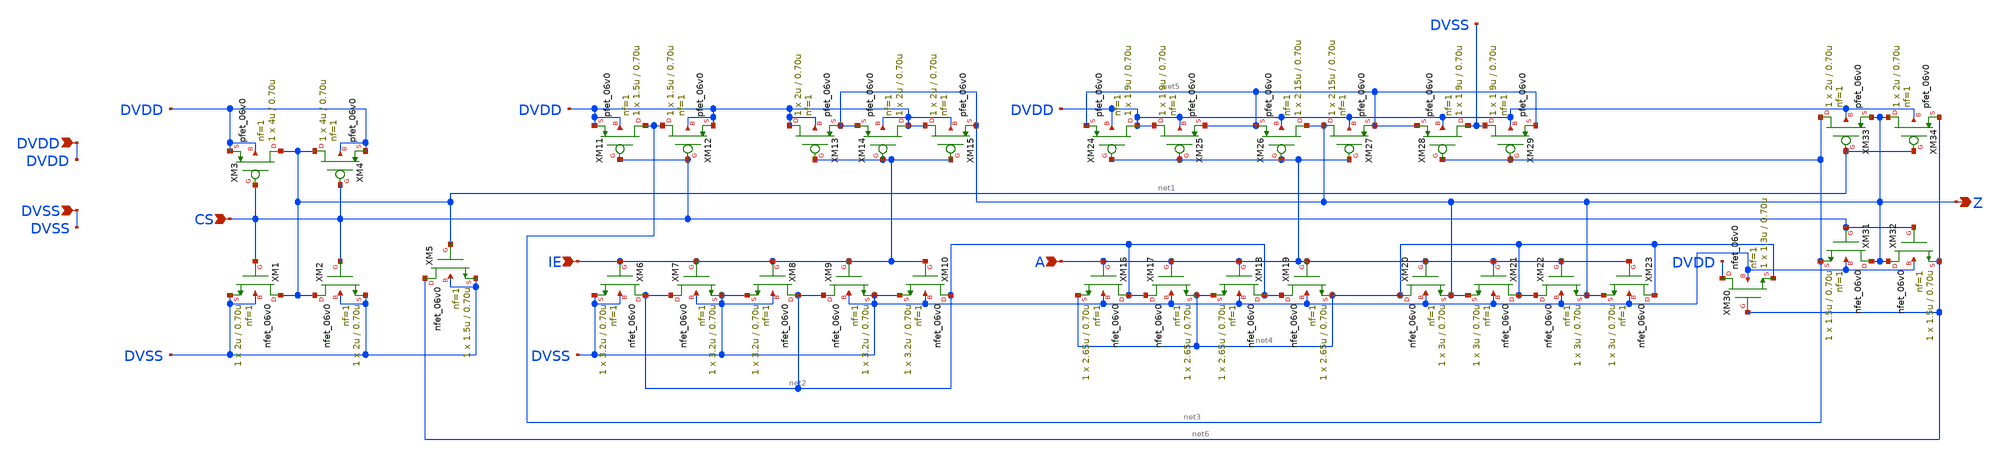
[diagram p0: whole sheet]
** sch_path: gf180mcu_fd_io__bi_24t/comp018green_in_cms_smt.sch
**.subckt comp018green_in_cms_smt CS IE Z A DVDD DVSS
*.ipin CS
*.ipin IE
*.opin Z
*.ipin A
*.ipin DVDD
*.ipin DVSS
XM1 net1 CS DVSS DVSS nfet_06v0 L=0.70u W=2u nf=1 ad='int((nf+1)/2) * W/nf * 0.18u' as='int((nf+2)/2) * W/nf * 0.18u'
+ pd='2*int((nf+1)/2) * (W/nf + 0.18u)' ps='2*int((nf+2)/2) * (W/nf + 0.18u)' nrd='0.18u / W' nrs='0.18u / W'
+ sa=0 sb=0 sd=0 m=1
XM2 net1 CS DVSS DVSS nfet_06v0 L=0.70u W=2u nf=1 ad='int((nf+1)/2) * W/nf * 0.18u' as='int((nf+2)/2) * W/nf * 0.18u'
+ pd='2*int((nf+1)/2) * (W/nf + 0.18u)' ps='2*int((nf+2)/2) * (W/nf + 0.18u)' nrd='0.18u / W' nrs='0.18u / W'
+ sa=0 sb=0 sd=0 m=1
XM3 net1 CS DVDD DVDD pfet_06v0 L=0.70u W=4u nf=1 ad='int((nf+1)/2) * W/nf * 0.18u' as='int((nf+2)/2) * W/nf * 0.18u'
+ pd='2*int((nf+1)/2) * (W/nf + 0.18u)' ps='2*int((nf+2)/2) * (W/nf + 0.18u)' nrd='0.18u / W' nrs='0.18u / W'
+ sa=0 sb=0 sd=0 m=1
XM4 net1 CS DVDD DVDD pfet_06v0 L=0.70u W=4u nf=1 ad='int((nf+1)/2) * W/nf * 0.18u' as='int((nf+2)/2) * W/nf * 0.18u'
+ pd='2*int((nf+1)/2) * (W/nf + 0.18u)' ps='2*int((nf+2)/2) * (W/nf + 0.18u)' nrd='0.18u / W' nrs='0.18u / W'
+ sa=0 sb=0 sd=0 m=1
XM5 net6 net1 DVSS DVSS nfet_06v0 L=0.70u W=1.5u nf=1 ad='int((nf+1)/2) * W/nf * 0.18u' as='int((nf+2)/2) * W/nf * 0.18u'
+ pd='2*int((nf+1)/2) * (W/nf + 0.18u)' ps='2*int((nf+2)/2) * (W/nf + 0.18u)' nrd='0.18u / W' nrs='0.18u / W'
+ sa=0 sb=0 sd=0 m=1
XM6 net2 IE DVSS DVSS nfet_06v0 L=0.70u W=3.2u nf=1 ad='int((nf+1)/2) * W/nf * 0.18u' as='int((nf+2)/2) * W/nf * 0.18u'
+ pd='2*int((nf+1)/2) * (W/nf + 0.18u)' ps='2*int((nf+2)/2) * (W/nf + 0.18u)' nrd='0.18u / W' nrs='0.18u / W'
+ sa=0 sb=0 sd=0 m=1
XM7 net2 IE DVSS DVSS nfet_06v0 L=0.70u W=3.2u nf=1 ad='int((nf+1)/2) * W/nf * 0.18u' as='int((nf+2)/2) * W/nf * 0.18u'
+ pd='2*int((nf+1)/2) * (W/nf + 0.18u)' ps='2*int((nf+2)/2) * (W/nf + 0.18u)' nrd='0.18u / W' nrs='0.18u / W'
+ sa=0 sb=0 sd=0 m=1
XM8 net2 IE DVSS DVSS nfet_06v0 L=0.70u W=3.2u nf=1 ad='int((nf+1)/2) * W/nf * 0.18u' as='int((nf+2)/2) * W/nf * 0.18u'
+ pd='2*int((nf+1)/2) * (W/nf + 0.18u)' ps='2*int((nf+2)/2) * (W/nf + 0.18u)' nrd='0.18u / W' nrs='0.18u / W'
+ sa=0 sb=0 sd=0 m=1
XM9 net2 IE DVSS DVSS nfet_06v0 L=0.70u W=3.2u nf=1 ad='int((nf+1)/2) * W/nf * 0.18u' as='int((nf+2)/2) * W/nf * 0.18u'
+ pd='2*int((nf+1)/2) * (W/nf + 0.18u)' ps='2*int((nf+2)/2) * (W/nf + 0.18u)' nrd='0.18u / W' nrs='0.18u / W'
+ sa=0 sb=0 sd=0 m=1
XM10 net2 IE DVSS DVSS nfet_06v0 L=0.70u W=3.2u nf=1 ad='int((nf+1)/2) * W/nf * 0.18u' as='int((nf+2)/2) * W/nf * 0.18u'
+ pd='2*int((nf+1)/2) * (W/nf + 0.18u)' ps='2*int((nf+2)/2) * (W/nf + 0.18u)' nrd='0.18u / W' nrs='0.18u / W'
+ sa=0 sb=0 sd=0 m=1
XM11 net3 CS DVDD DVDD pfet_06v0 L=0.70u W=1.5u nf=1 ad='int((nf+1)/2) * W/nf * 0.18u' as='int((nf+2)/2) * W/nf * 0.18u'
+ pd='2*int((nf+1)/2) * (W/nf + 0.18u)' ps='2*int((nf+2)/2) * (W/nf + 0.18u)' nrd='0.18u / W' nrs='0.18u / W'
+ sa=0 sb=0 sd=0 m=1
XM12 net3 CS DVDD DVDD pfet_06v0 L=0.70u W=1.5u nf=1 ad='int((nf+1)/2) * W/nf * 0.18u' as='int((nf+2)/2) * W/nf * 0.18u'
+ pd='2*int((nf+1)/2) * (W/nf + 0.18u)' ps='2*int((nf+2)/2) * (W/nf + 0.18u)' nrd='0.18u / W' nrs='0.18u / W'
+ sa=0 sb=0 sd=0 m=1
XM13 DVDD IE Z DVDD pfet_06v0 L=0.70u W=2u nf=1 ad='int((nf+1)/2) * W/nf * 0.18u' as='int((nf+2)/2) * W/nf * 0.18u'
+ pd='2*int((nf+1)/2) * (W/nf + 0.18u)' ps='2*int((nf+2)/2) * (W/nf + 0.18u)' nrd='0.18u / W' nrs='0.18u / W'
+ sa=0 sb=0 sd=0 m=1
XM14 DVDD IE Z DVDD pfet_06v0 L=0.70u W=2u nf=1 ad='int((nf+1)/2) * W/nf * 0.18u' as='int((nf+2)/2) * W/nf * 0.18u'
+ pd='2*int((nf+1)/2) * (W/nf + 0.18u)' ps='2*int((nf+2)/2) * (W/nf + 0.18u)' nrd='0.18u / W' nrs='0.18u / W'
+ sa=0 sb=0 sd=0 m=1
XM15 DVDD IE Z DVDD pfet_06v0 L=0.70u W=2u nf=1 ad='int((nf+1)/2) * W/nf * 0.18u' as='int((nf+2)/2) * W/nf * 0.18u'
+ pd='2*int((nf+1)/2) * (W/nf + 0.18u)' ps='2*int((nf+2)/2) * (W/nf + 0.18u)' nrd='0.18u / W' nrs='0.18u / W'
+ sa=0 sb=0 sd=0 m=1
XM16 net2 A net4 DVSS nfet_06v0 L=0.70u W=2.65u nf=1 ad='int((nf+1)/2) * W/nf * 0.18u' as='int((nf+2)/2) * W/nf * 0.18u'
+ pd='2*int((nf+1)/2) * (W/nf + 0.18u)' ps='2*int((nf+2)/2) * (W/nf + 0.18u)' nrd='0.18u / W' nrs='0.18u / W'
+ sa=0 sb=0 sd=0 m=1
XM17 net2 A net4 DVSS nfet_06v0 L=0.70u W=2.65u nf=1 ad='int((nf+1)/2) * W/nf * 0.18u' as='int((nf+2)/2) * W/nf * 0.18u'
+ pd='2*int((nf+1)/2) * (W/nf + 0.18u)' ps='2*int((nf+2)/2) * (W/nf + 0.18u)' nrd='0.18u / W' nrs='0.18u / W'
+ sa=0 sb=0 sd=0 m=1
XM18 net2 A net4 DVSS nfet_06v0 L=0.70u W=2.65u nf=1 ad='int((nf+1)/2) * W/nf * 0.18u' as='int((nf+2)/2) * W/nf * 0.18u'
+ pd='2*int((nf+1)/2) * (W/nf + 0.18u)' ps='2*int((nf+2)/2) * (W/nf + 0.18u)' nrd='0.18u / W' nrs='0.18u / W'
+ sa=0 sb=0 sd=0 m=1
XM19 net2 A net4 DVSS nfet_06v0 L=0.70u W=2.65u nf=1 ad='int((nf+1)/2) * W/nf * 0.18u' as='int((nf+2)/2) * W/nf * 0.18u'
+ pd='2*int((nf+1)/2) * (W/nf + 0.18u)' ps='2*int((nf+2)/2) * (W/nf + 0.18u)' nrd='0.18u / W' nrs='0.18u / W'
+ sa=0 sb=0 sd=0 m=1
XM20 net4 A Z DVSS nfet_06v0 L=0.70u W=3u nf=1 ad='int((nf+1)/2) * W/nf * 0.18u' as='int((nf+2)/2) * W/nf * 0.18u'
+ pd='2*int((nf+1)/2) * (W/nf + 0.18u)' ps='2*int((nf+2)/2) * (W/nf + 0.18u)' nrd='0.18u / W' nrs='0.18u / W'
+ sa=0 sb=0 sd=0 m=1
XM21 net4 A Z DVSS nfet_06v0 L=0.70u W=3u nf=1 ad='int((nf+1)/2) * W/nf * 0.18u' as='int((nf+2)/2) * W/nf * 0.18u'
+ pd='2*int((nf+1)/2) * (W/nf + 0.18u)' ps='2*int((nf+2)/2) * (W/nf + 0.18u)' nrd='0.18u / W' nrs='0.18u / W'
+ sa=0 sb=0 sd=0 m=1
XM22 net4 A Z DVSS nfet_06v0 L=0.70u W=3u nf=1 ad='int((nf+1)/2) * W/nf * 0.18u' as='int((nf+2)/2) * W/nf * 0.18u'
+ pd='2*int((nf+1)/2) * (W/nf + 0.18u)' ps='2*int((nf+2)/2) * (W/nf + 0.18u)' nrd='0.18u / W' nrs='0.18u / W'
+ sa=0 sb=0 sd=0 m=1
XM23 net4 A Z DVSS nfet_06v0 L=0.70u W=3u nf=1 ad='int((nf+1)/2) * W/nf * 0.18u' as='int((nf+2)/2) * W/nf * 0.18u'
+ pd='2*int((nf+1)/2) * (W/nf + 0.18u)' ps='2*int((nf+2)/2) * (W/nf + 0.18u)' nrd='0.18u / W' nrs='0.18u / W'
+ sa=0 sb=0 sd=0 m=1
XM24 DVDD A net5 DVDD pfet_06v0 L=0.70u W=1.9u nf=1 ad='int((nf+1)/2) * W/nf * 0.18u' as='int((nf+2)/2) * W/nf * 0.18u'
+ pd='2*int((nf+1)/2) * (W/nf + 0.18u)' ps='2*int((nf+2)/2) * (W/nf + 0.18u)' nrd='0.18u / W' nrs='0.18u / W'
+ sa=0 sb=0 sd=0 m=1
XM25 DVDD A net5 DVDD pfet_06v0 L=0.70u W=1.9u nf=1 ad='int((nf+1)/2) * W/nf * 0.18u' as='int((nf+2)/2) * W/nf * 0.18u'
+ pd='2*int((nf+1)/2) * (W/nf + 0.18u)' ps='2*int((nf+2)/2) * (W/nf + 0.18u)' nrd='0.18u / W' nrs='0.18u / W'
+ sa=0 sb=0 sd=0 m=1
XM26 Z A net5 DVDD pfet_06v0 L=0.70u W=2.15u nf=1 ad='int((nf+1)/2) * W/nf * 0.18u' as='int((nf+2)/2) * W/nf * 0.18u'
+ pd='2*int((nf+1)/2) * (W/nf + 0.18u)' ps='2*int((nf+2)/2) * (W/nf + 0.18u)' nrd='0.18u / W' nrs='0.18u / W'
+ sa=0 sb=0 sd=0 m=1
XM27 Z A net5 DVDD pfet_06v0 L=0.70u W=2.15u nf=1 ad='int((nf+1)/2) * W/nf * 0.18u' as='int((nf+2)/2) * W/nf * 0.18u'
+ pd='2*int((nf+1)/2) * (W/nf + 0.18u)' ps='2*int((nf+2)/2) * (W/nf + 0.18u)' nrd='0.18u / W' nrs='0.18u / W'
+ sa=0 sb=0 sd=0 m=1
XM28 DVSS net3 net5 DVDD pfet_06v0 L=0.70u W=1.9u nf=1 ad='int((nf+1)/2) * W/nf * 0.18u' as='int((nf+2)/2) * W/nf * 0.18u'
+ pd='2*int((nf+1)/2) * (W/nf + 0.18u)' ps='2*int((nf+2)/2) * (W/nf + 0.18u)' nrd='0.18u / W' nrs='0.18u / W'
+ sa=0 sb=0 sd=0 m=1
XM29 DVSS net3 net5 DVDD pfet_06v0 L=0.70u W=1.9u nf=1 ad='int((nf+1)/2) * W/nf * 0.18u' as='int((nf+2)/2) * W/nf * 0.18u'
+ pd='2*int((nf+1)/2) * (W/nf + 0.18u)' ps='2*int((nf+2)/2) * (W/nf + 0.18u)' nrd='0.18u / W' nrs='0.18u / W'
+ sa=0 sb=0 sd=0 m=1
XM30 DVDD net6 net4 DVSS nfet_06v0 L=0.70u W=1.3u nf=1 ad='int((nf+1)/2) * W/nf * 0.18u' as='int((nf+2)/2) * W/nf * 0.18u'
+ pd='2*int((nf+1)/2) * (W/nf + 0.18u)' ps='2*int((nf+2)/2) * (W/nf + 0.18u)' nrd='0.18u / W' nrs='0.18u / W'
+ sa=0 sb=0 sd=0 m=1
XM31 Z CS net3 DVSS nfet_06v0 L=0.70u W=1.5u nf=1 ad='int((nf+1)/2) * W/nf * 0.18u' as='int((nf+2)/2) * W/nf * 0.18u'
+ pd='2*int((nf+1)/2) * (W/nf + 0.18u)' ps='2*int((nf+2)/2) * (W/nf + 0.18u)' nrd='0.18u / W' nrs='0.18u / W'
+ sa=0 sb=0 sd=0 m=1
XM32 Z CS net6 DVSS nfet_06v0 L=0.70u W=1.5u nf=1 ad='int((nf+1)/2) * W/nf * 0.18u' as='int((nf+2)/2) * W/nf * 0.18u'
+ pd='2*int((nf+1)/2) * (W/nf + 0.18u)' ps='2*int((nf+2)/2) * (W/nf + 0.18u)' nrd='0.18u / W' nrs='0.18u / W'
+ sa=0 sb=0 sd=0 m=1
XM33 net3 net1 Z DVDD pfet_06v0 L=0.70u W=2u nf=1 ad='int((nf+1)/2) * W/nf * 0.18u' as='int((nf+2)/2) * W/nf * 0.18u'
+ pd='2*int((nf+1)/2) * (W/nf + 0.18u)' ps='2*int((nf+2)/2) * (W/nf + 0.18u)' nrd='0.18u / W' nrs='0.18u / W'
+ sa=0 sb=0 sd=0 m=1
XM34 Z net1 net6 DVDD pfet_06v0 L=0.70u W=2u nf=1 ad='int((nf+1)/2) * W/nf * 0.18u' as='int((nf+2)/2) * W/nf * 0.18u'
+ pd='2*int((nf+1)/2) * (W/nf + 0.18u)' ps='2*int((nf+2)/2) * (W/nf + 0.18u)' nrd='0.18u / W' nrs='0.18u / W'
+ sa=0 sb=0 sd=0 m=1
**.ends
.end
